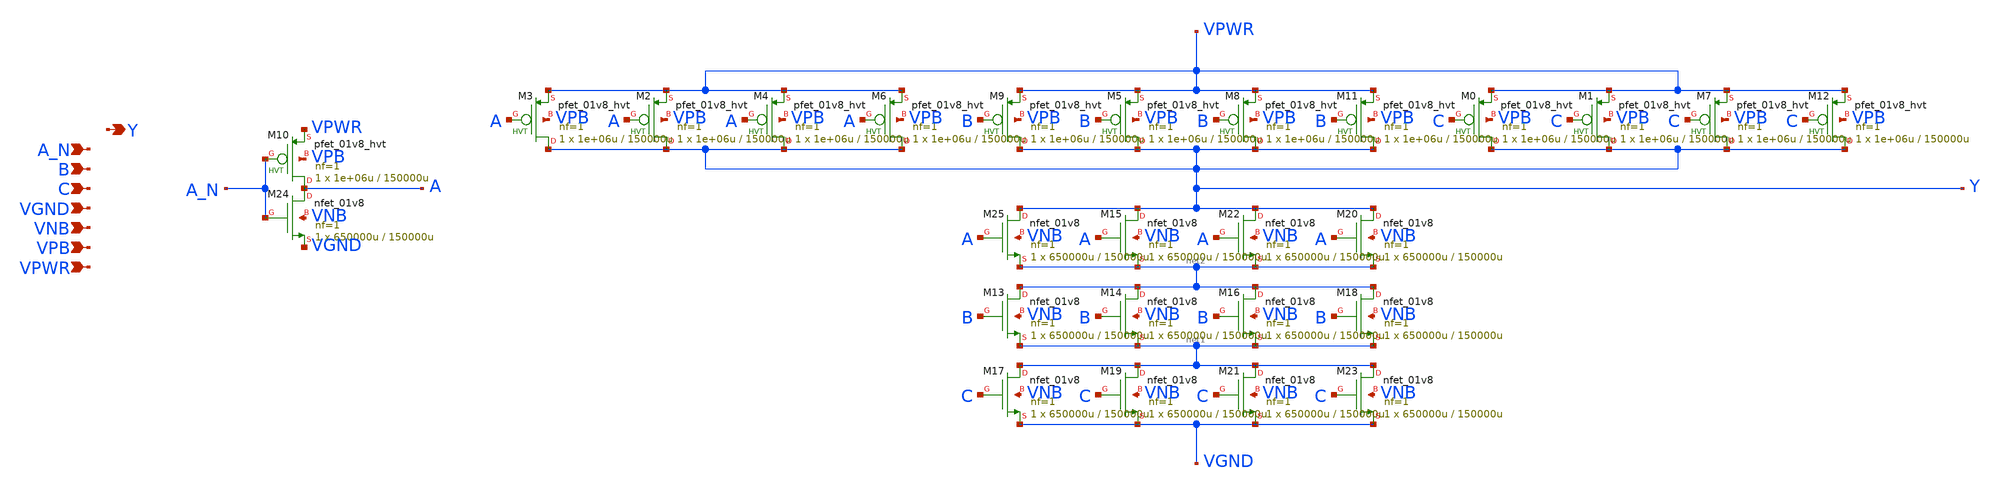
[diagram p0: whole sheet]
** sch_path: schematics/nand3b/sky130_fd_sc_hd__nand3b_4.sch
**.subckt sky130_fd_sc_hd__nand3b_4 A_N B C VGND VNB VPB VPWR Y
*.ipin A_N
*.ipin B
*.ipin C
*.ipin VGND
*.ipin VNB
*.ipin VPB
*.ipin VPWR
*.opin Y
XM0 Y C VPWR VPB sky130_fd_pr__pfet_01v8_hvt L=150000u W=1e+06u nf=1 ad='int((1 + 1)/2) * 1e+06u / 1 * 0.29'
+ as='int((1 + 2)/2) * 1e+06u / 1 * 0.29' pd='2*int((1 + 1)/2) * (1e+06u / 1 + 0.29)' ps='2*int((1 + 2)/2) * (1e+06u / 1 + 0.29)'
+ nrd='0.29 / 1e+06u ' nrs='0.29 / 1e+06u ' sa=0 sb=0 sd=0 mult=1 m=1
XM1 Y C VPWR VPB sky130_fd_pr__pfet_01v8_hvt L=150000u W=1e+06u nf=1 ad='int((1 + 1)/2) * 1e+06u / 1 * 0.29'
+ as='int((1 + 2)/2) * 1e+06u / 1 * 0.29' pd='2*int((1 + 1)/2) * (1e+06u / 1 + 0.29)' ps='2*int((1 + 2)/2) * (1e+06u / 1 + 0.29)'
+ nrd='0.29 / 1e+06u ' nrs='0.29 / 1e+06u ' sa=0 sb=0 sd=0 mult=1 m=1
XM2 Y A VPWR VPB sky130_fd_pr__pfet_01v8_hvt L=150000u W=1e+06u nf=1 ad='int((1 + 1)/2) * 1e+06u / 1 * 0.29'
+ as='int((1 + 2)/2) * 1e+06u / 1 * 0.29' pd='2*int((1 + 1)/2) * (1e+06u / 1 + 0.29)' ps='2*int((1 + 2)/2) * (1e+06u / 1 + 0.29)'
+ nrd='0.29 / 1e+06u ' nrs='0.29 / 1e+06u ' sa=0 sb=0 sd=0 mult=1 m=1
XM3 Y A VPWR VPB sky130_fd_pr__pfet_01v8_hvt L=150000u W=1e+06u nf=1 ad='int((1 + 1)/2) * 1e+06u / 1 * 0.29'
+ as='int((1 + 2)/2) * 1e+06u / 1 * 0.29' pd='2*int((1 + 1)/2) * (1e+06u / 1 + 0.29)' ps='2*int((1 + 2)/2) * (1e+06u / 1 + 0.29)'
+ nrd='0.29 / 1e+06u ' nrs='0.29 / 1e+06u ' sa=0 sb=0 sd=0 mult=1 m=1
XM4 Y A VPWR VPB sky130_fd_pr__pfet_01v8_hvt L=150000u W=1e+06u nf=1 ad='int((1 + 1)/2) * 1e+06u / 1 * 0.29'
+ as='int((1 + 2)/2) * 1e+06u / 1 * 0.29' pd='2*int((1 + 1)/2) * (1e+06u / 1 + 0.29)' ps='2*int((1 + 2)/2) * (1e+06u / 1 + 0.29)'
+ nrd='0.29 / 1e+06u ' nrs='0.29 / 1e+06u ' sa=0 sb=0 sd=0 mult=1 m=1
XM5 Y B VPWR VPB sky130_fd_pr__pfet_01v8_hvt L=150000u W=1e+06u nf=1 ad='int((1 + 1)/2) * 1e+06u / 1 * 0.29'
+ as='int((1 + 2)/2) * 1e+06u / 1 * 0.29' pd='2*int((1 + 1)/2) * (1e+06u / 1 + 0.29)' ps='2*int((1 + 2)/2) * (1e+06u / 1 + 0.29)'
+ nrd='0.29 / 1e+06u ' nrs='0.29 / 1e+06u ' sa=0 sb=0 sd=0 mult=1 m=1
XM6 Y A VPWR VPB sky130_fd_pr__pfet_01v8_hvt L=150000u W=1e+06u nf=1 ad='int((1 + 1)/2) * 1e+06u / 1 * 0.29'
+ as='int((1 + 2)/2) * 1e+06u / 1 * 0.29' pd='2*int((1 + 1)/2) * (1e+06u / 1 + 0.29)' ps='2*int((1 + 2)/2) * (1e+06u / 1 + 0.29)'
+ nrd='0.29 / 1e+06u ' nrs='0.29 / 1e+06u ' sa=0 sb=0 sd=0 mult=1 m=1
XM7 Y C VPWR VPB sky130_fd_pr__pfet_01v8_hvt L=150000u W=1e+06u nf=1 ad='int((1 + 1)/2) * 1e+06u / 1 * 0.29'
+ as='int((1 + 2)/2) * 1e+06u / 1 * 0.29' pd='2*int((1 + 1)/2) * (1e+06u / 1 + 0.29)' ps='2*int((1 + 2)/2) * (1e+06u / 1 + 0.29)'
+ nrd='0.29 / 1e+06u ' nrs='0.29 / 1e+06u ' sa=0 sb=0 sd=0 mult=1 m=1
XM8 Y B VPWR VPB sky130_fd_pr__pfet_01v8_hvt L=150000u W=1e+06u nf=1 ad='int((1 + 1)/2) * 1e+06u / 1 * 0.29'
+ as='int((1 + 2)/2) * 1e+06u / 1 * 0.29' pd='2*int((1 + 1)/2) * (1e+06u / 1 + 0.29)' ps='2*int((1 + 2)/2) * (1e+06u / 1 + 0.29)'
+ nrd='0.29 / 1e+06u ' nrs='0.29 / 1e+06u ' sa=0 sb=0 sd=0 mult=1 m=1
XM9 Y B VPWR VPB sky130_fd_pr__pfet_01v8_hvt L=150000u W=1e+06u nf=1 ad='int((1 + 1)/2) * 1e+06u / 1 * 0.29'
+ as='int((1 + 2)/2) * 1e+06u / 1 * 0.29' pd='2*int((1 + 1)/2) * (1e+06u / 1 + 0.29)' ps='2*int((1 + 2)/2) * (1e+06u / 1 + 0.29)'
+ nrd='0.29 / 1e+06u ' nrs='0.29 / 1e+06u ' sa=0 sb=0 sd=0 mult=1 m=1
XM10 A A_N VPWR VPB sky130_fd_pr__pfet_01v8_hvt L=150000u W=1e+06u nf=1 ad='int((1 + 1)/2) * 1e+06u / 1 * 0.29'
+ as='int((1 + 2)/2) * 1e+06u / 1 * 0.29' pd='2*int((1 + 1)/2) * (1e+06u / 1 + 0.29)' ps='2*int((1 + 2)/2) * (1e+06u / 1 + 0.29)'
+ nrd='0.29 / 1e+06u ' nrs='0.29 / 1e+06u ' sa=0 sb=0 sd=0 mult=1 m=1
XM11 Y B VPWR VPB sky130_fd_pr__pfet_01v8_hvt L=150000u W=1e+06u nf=1 ad='int((1 + 1)/2) * 1e+06u / 1 * 0.29'
+ as='int((1 + 2)/2) * 1e+06u / 1 * 0.29' pd='2*int((1 + 1)/2) * (1e+06u / 1 + 0.29)' ps='2*int((1 + 2)/2) * (1e+06u / 1 + 0.29)'
+ nrd='0.29 / 1e+06u ' nrs='0.29 / 1e+06u ' sa=0 sb=0 sd=0 mult=1 m=1
XM12 Y C VPWR VPB sky130_fd_pr__pfet_01v8_hvt L=150000u W=1e+06u nf=1 ad='int((1 + 1)/2) * 1e+06u / 1 * 0.29'
+ as='int((1 + 2)/2) * 1e+06u / 1 * 0.29' pd='2*int((1 + 1)/2) * (1e+06u / 1 + 0.29)' ps='2*int((1 + 2)/2) * (1e+06u / 1 + 0.29)'
+ nrd='0.29 / 1e+06u ' nrs='0.29 / 1e+06u ' sa=0 sb=0 sd=0 mult=1 m=1
XM13 net2 B net1 VNB sky130_fd_pr__nfet_01v8 L=150000u W=650000u nf=1 ad='int((1 + 1)/2) * 650000u / 1 * 0.29'
+ as='int((1 + 2)/2) * 650000u / 1 * 0.29' pd='2*int((1 + 1)/2) * (650000u / 1 + 0.29)' ps='2*int((1 + 2)/2) * (650000u / 1 + 0.29)'
+ nrd='0.29 / 650000u ' nrs='0.29 / 650000u ' sa=0 sb=0 sd=0 mult=1 m=1
XM14 net2 B net1 VNB sky130_fd_pr__nfet_01v8 L=150000u W=650000u nf=1 ad='int((1 + 1)/2) * 650000u / 1 * 0.29'
+ as='int((1 + 2)/2) * 650000u / 1 * 0.29' pd='2*int((1 + 1)/2) * (650000u / 1 + 0.29)' ps='2*int((1 + 2)/2) * (650000u / 1 + 0.29)'
+ nrd='0.29 / 650000u ' nrs='0.29 / 650000u ' sa=0 sb=0 sd=0 mult=1 m=1
XM15 Y A net2 VNB sky130_fd_pr__nfet_01v8 L=150000u W=650000u nf=1 ad='int((1 + 1)/2) * 650000u / 1 * 0.29'
+ as='int((1 + 2)/2) * 650000u / 1 * 0.29' pd='2*int((1 + 1)/2) * (650000u / 1 + 0.29)' ps='2*int((1 + 2)/2) * (650000u / 1 + 0.29)'
+ nrd='0.29 / 650000u ' nrs='0.29 / 650000u ' sa=0 sb=0 sd=0 mult=1 m=1
XM16 net2 B net1 VNB sky130_fd_pr__nfet_01v8 L=150000u W=650000u nf=1 ad='int((1 + 1)/2) * 650000u / 1 * 0.29'
+ as='int((1 + 2)/2) * 650000u / 1 * 0.29' pd='2*int((1 + 1)/2) * (650000u / 1 + 0.29)' ps='2*int((1 + 2)/2) * (650000u / 1 + 0.29)'
+ nrd='0.29 / 650000u ' nrs='0.29 / 650000u ' sa=0 sb=0 sd=0 mult=1 m=1
XM17 net1 C VGND VNB sky130_fd_pr__nfet_01v8 L=150000u W=650000u nf=1 ad='int((1 + 1)/2) * 650000u / 1 * 0.29'
+ as='int((1 + 2)/2) * 650000u / 1 * 0.29' pd='2*int((1 + 1)/2) * (650000u / 1 + 0.29)' ps='2*int((1 + 2)/2) * (650000u / 1 + 0.29)'
+ nrd='0.29 / 650000u ' nrs='0.29 / 650000u ' sa=0 sb=0 sd=0 mult=1 m=1
XM18 net2 B net1 VNB sky130_fd_pr__nfet_01v8 L=150000u W=650000u nf=1 ad='int((1 + 1)/2) * 650000u / 1 * 0.29'
+ as='int((1 + 2)/2) * 650000u / 1 * 0.29' pd='2*int((1 + 1)/2) * (650000u / 1 + 0.29)' ps='2*int((1 + 2)/2) * (650000u / 1 + 0.29)'
+ nrd='0.29 / 650000u ' nrs='0.29 / 650000u ' sa=0 sb=0 sd=0 mult=1 m=1
XM19 net1 C VGND VNB sky130_fd_pr__nfet_01v8 L=150000u W=650000u nf=1 ad='int((1 + 1)/2) * 650000u / 1 * 0.29'
+ as='int((1 + 2)/2) * 650000u / 1 * 0.29' pd='2*int((1 + 1)/2) * (650000u / 1 + 0.29)' ps='2*int((1 + 2)/2) * (650000u / 1 + 0.29)'
+ nrd='0.29 / 650000u ' nrs='0.29 / 650000u ' sa=0 sb=0 sd=0 mult=1 m=1
XM20 Y A net2 VNB sky130_fd_pr__nfet_01v8 L=150000u W=650000u nf=1 ad='int((1 + 1)/2) * 650000u / 1 * 0.29'
+ as='int((1 + 2)/2) * 650000u / 1 * 0.29' pd='2*int((1 + 1)/2) * (650000u / 1 + 0.29)' ps='2*int((1 + 2)/2) * (650000u / 1 + 0.29)'
+ nrd='0.29 / 650000u ' nrs='0.29 / 650000u ' sa=0 sb=0 sd=0 mult=1 m=1
XM21 net1 C VGND VNB sky130_fd_pr__nfet_01v8 L=150000u W=650000u nf=1 ad='int((1 + 1)/2) * 650000u / 1 * 0.29'
+ as='int((1 + 2)/2) * 650000u / 1 * 0.29' pd='2*int((1 + 1)/2) * (650000u / 1 + 0.29)' ps='2*int((1 + 2)/2) * (650000u / 1 + 0.29)'
+ nrd='0.29 / 650000u ' nrs='0.29 / 650000u ' sa=0 sb=0 sd=0 mult=1 m=1
XM22 Y A net2 VNB sky130_fd_pr__nfet_01v8 L=150000u W=650000u nf=1 ad='int((1 + 1)/2) * 650000u / 1 * 0.29'
+ as='int((1 + 2)/2) * 650000u / 1 * 0.29' pd='2*int((1 + 1)/2) * (650000u / 1 + 0.29)' ps='2*int((1 + 2)/2) * (650000u / 1 + 0.29)'
+ nrd='0.29 / 650000u ' nrs='0.29 / 650000u ' sa=0 sb=0 sd=0 mult=1 m=1
XM23 net1 C VGND VNB sky130_fd_pr__nfet_01v8 L=150000u W=650000u nf=1 ad='int((1 + 1)/2) * 650000u / 1 * 0.29'
+ as='int((1 + 2)/2) * 650000u / 1 * 0.29' pd='2*int((1 + 1)/2) * (650000u / 1 + 0.29)' ps='2*int((1 + 2)/2) * (650000u / 1 + 0.29)'
+ nrd='0.29 / 650000u ' nrs='0.29 / 650000u ' sa=0 sb=0 sd=0 mult=1 m=1
XM25 Y A net2 VNB sky130_fd_pr__nfet_01v8 L=150000u W=650000u nf=1 ad='int((1 + 1)/2) * 650000u / 1 * 0.29'
+ as='int((1 + 2)/2) * 650000u / 1 * 0.29' pd='2*int((1 + 1)/2) * (650000u / 1 + 0.29)' ps='2*int((1 + 2)/2) * (650000u / 1 + 0.29)'
+ nrd='0.29 / 650000u ' nrs='0.29 / 650000u ' sa=0 sb=0 sd=0 mult=1 m=1
XM24 A A_N VGND VNB sky130_fd_pr__nfet_01v8 L=150000u W=650000u nf=1 ad='int((1 + 1)/2) * 650000u / 1 * 0.29'
+ as='int((1 + 2)/2) * 650000u / 1 * 0.29' pd='2*int((1 + 1)/2) * (650000u / 1 + 0.29)' ps='2*int((1 + 2)/2) * (650000u / 1 + 0.29)'
+ nrd='0.29 / 650000u ' nrs='0.29 / 650000u ' sa=0 sb=0 sd=0 mult=1 m=1
**.ends
.end
